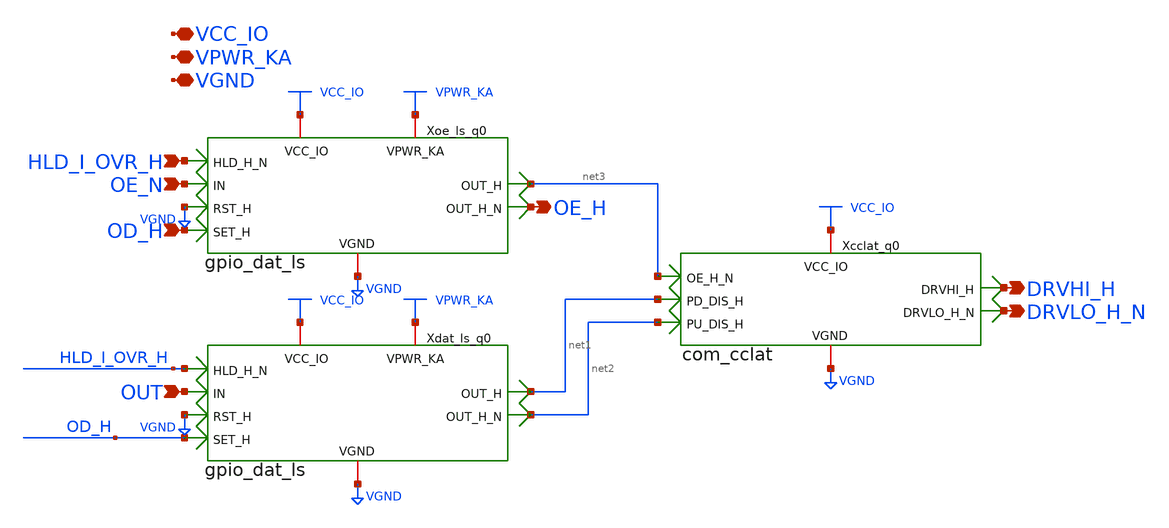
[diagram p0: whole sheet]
** sch_path: gpiov2_opath_datoe.sch
* Copyright 2023 David Mitchell Bailey
* Licensed under the Apache License, Version 2.0 (the "License");
* you may not use this file except in compliance with the License.
* You may obtain a copy of the License at
* https://www.apache.org/licenses/LICENSE-2.0
* Unless required by applicable law or agreed to in writing, software
* distributed under the License is distributed on an "AS IS" BASIS,
* WITHOUT WARRANTIES OR CONDITIONS OF ANY KIND, either express or implied.
* See the License for the specific language governing permissions and
* limitations under the License.
**.subckt gpiov2_opath_datoe VCC_IO DRVHI_H OUT HLD_I_OVR_H OE_N OD_H DRVLO_H_N OE_H VPWR_KA VGND
*.iopin VCC_IO
*.opin DRVHI_H
*.ipin OUT
*.ipin HLD_I_OVR_H
*.ipin OE_N
*.ipin OD_H
*.opin DRVLO_H_N
*.opin OE_H
*.iopin VPWR_KA
*.iopin VGND
Xdat_ls_q0 VCC_IO VPWR_KA VGND net1 net2 HLD_I_OVR_H OD_H VGND OUT gpio_dat_ls
Xcclat_q0 VCC_IO VGND DRVHI_H net2 net3 DRVLO_H_N net1 com_cclat
Xoe_ls_q0 VCC_IO VPWR_KA VGND net3 OE_H HLD_I_OVR_H OD_H VGND OE_N gpio_dat_ls
**.ends

* expanding   symbol:  gpio_dat_ls.sym # of pins=9
** sym_path: gpio_dat_ls.sym
** sch_path: gpio_dat_ls.sch
.subckt gpio_dat_ls VCC_IO VPWR_KA VGND OUT_H OUT_H_N HLD_H_N SET_H RST_H IN
*.ipin IN
*.ipin HLD_H_N
*.ipin SET_H
*.ipin RST_H
*.opin OUT_H_N
*.opin OUT_H
*.iopin VCC_IO
*.iopin VPWR_KA
*.iopin VGND
XM1 fbk fbk_n VGND VGND sky130_fd_pr__nfet_g5v0d10v5 L=0.6 W=0.7 nf=1 ad='int((nf+1)/2) * W/nf * 0.29'
+ as='int((nf+2)/2) * W/nf * 0.29' pd='2*int((nf+1)/2) * (W/nf + 0.29)' ps='2*int((nf+2)/2) * (W/nf + 0.29)'
+ nrd='0.29 / W' nrs='0.29 / W' sa=0 sb=0 sd=0 mult=1 m=1
XM2 fbk_n fbk VGND VGND sky130_fd_pr__nfet_g5v0d10v5 L=0.6 W=0.7 nf=1 ad='int((nf+1)/2) * W/nf * 0.29'
+ as='int((nf+2)/2) * W/nf * 0.29' pd='2*int((nf+1)/2) * (W/nf + 0.29)' ps='2*int((nf+2)/2) * (W/nf + 0.29)'
+ nrd='0.29 / W' nrs='0.29 / W' sa=0 sb=0 sd=0 mult=1 m=1
XM3 fbk fbk_n VCC_IO VCC_IO sky130_fd_pr__pfet_g5v0d10v5 L=0.5 W=1 nf=1 ad='int((nf+1)/2) * W/nf * 0.29'
+ as='int((nf+2)/2) * W/nf * 0.29' pd='2*int((nf+1)/2) * (W/nf + 0.29)' ps='2*int((nf+2)/2) * (W/nf + 0.29)'
+ nrd='0.29 / W' nrs='0.29 / W' sa=0 sb=0 sd=0 mult=1 m=1
XM4 fbk_n fbk VCC_IO VCC_IO sky130_fd_pr__pfet_g5v0d10v5 L=0.5 W=1 nf=1 ad='int((nf+1)/2) * W/nf * 0.29'
+ as='int((nf+2)/2) * W/nf * 0.29' pd='2*int((nf+1)/2) * (W/nf + 0.29)' ps='2*int((nf+2)/2) * (W/nf + 0.29)'
+ nrd='0.29 / W' nrs='0.29 / W' sa=0 sb=0 sd=0 mult=1 m=1
XM5 fbk HLD_H_N net3 VGND sky130_fd_pr__nfet_g5v0d10v5 L=0.5 W=5 nf=1 ad='int((nf+1)/2) * W/nf * 0.29'
+ as='int((nf+2)/2) * W/nf * 0.29' pd='2*int((nf+1)/2) * (W/nf + 0.29)' ps='2*int((nf+2)/2) * (W/nf + 0.29)'
+ nrd='0.29 / W' nrs='0.29 / W' sa=0 sb=0 sd=0 mult=1 m=1
XM6 net3 VPWR_KA net4 VGND sky130_fd_pr__nfet_05v0_nvt L=0.9 W=1 nf=1 ad='int((nf+1)/2) * W/nf * 0.29'
+ as='int((nf+2)/2) * W/nf * 0.29' pd='2*int((nf+1)/2) * (W/nf + 0.29)' ps='2*int((nf+2)/2) * (W/nf + 0.29)'
+ nrd='0.29 / W' nrs='0.29 / W' sa=0 sb=0 sd=0 mult=8 m=8
XM7 net4 net2 VGND VGND sky130_fd_pr__nfet_01v8_lvt L=0.15 W=8 nf=1 ad='int((nf+1)/2) * W/nf * 0.29'
+ as='int((nf+2)/2) * W/nf * 0.29' pd='2*int((nf+1)/2) * (W/nf + 0.29)' ps='2*int((nf+2)/2) * (W/nf + 0.29)'
+ nrd='0.29 / W' nrs='0.29 / W' sa=0 sb=0 sd=0 mult=1 m=1
XM8 fbk_n HLD_H_N net5 VGND sky130_fd_pr__nfet_g5v0d10v5 L=0.5 W=5 nf=1 ad='int((nf+1)/2) * W/nf * 0.29'
+ as='int((nf+2)/2) * W/nf * 0.29' pd='2*int((nf+1)/2) * (W/nf + 0.29)' ps='2*int((nf+2)/2) * (W/nf + 0.29)'
+ nrd='0.29 / W' nrs='0.29 / W' sa=0 sb=0 sd=0 mult=1 m=1
XM9 net5 VPWR_KA net6 VGND sky130_fd_pr__nfet_05v0_nvt L=0.9 W=1 nf=1 ad='int((nf+1)/2) * W/nf * 0.29'
+ as='int((nf+2)/2) * W/nf * 0.29' pd='2*int((nf+1)/2) * (W/nf + 0.29)' ps='2*int((nf+2)/2) * (W/nf + 0.29)'
+ nrd='0.29 / W' nrs='0.29 / W' sa=0 sb=0 sd=0 mult=8 m=8
XM10 net6 net1 VGND VGND sky130_fd_pr__nfet_01v8_lvt L=0.15 W=8 nf=1 ad='int((nf+1)/2) * W/nf * 0.29'
+ as='int((nf+2)/2) * W/nf * 0.29' pd='2*int((nf+1)/2) * (W/nf + 0.29)' ps='2*int((nf+2)/2) * (W/nf + 0.29)'
+ nrd='0.29 / W' nrs='0.29 / W' sa=0 sb=0 sd=0 mult=1 m=1
XM11 fbk SET_H VGND VGND sky130_fd_pr__nfet_g5v0d10v5 L=0.6 W=3 nf=1 ad='int((nf+1)/2) * W/nf * 0.29'
+ as='int((nf+2)/2) * W/nf * 0.29' pd='2*int((nf+1)/2) * (W/nf + 0.29)' ps='2*int((nf+2)/2) * (W/nf + 0.29)'
+ nrd='0.29 / W' nrs='0.29 / W' sa=0 sb=0 sd=0 mult=1 m=1
XM12 net1 IN VGND VGND sky130_fd_pr__nfet_01v8 L=0.25 W=1 nf=1 ad='int((nf+1)/2) * W/nf * 0.29' as='int((nf+2)/2) * W/nf * 0.29'
+ pd='2*int((nf+1)/2) * (W/nf + 0.29)' ps='2*int((nf+2)/2) * (W/nf + 0.29)' nrd='0.29 / W' nrs='0.29 / W'
+ sa=0 sb=0 sd=0 mult=2 m=2
XM14 net2 net1 VGND VGND sky130_fd_pr__nfet_01v8 L=0.25 W=1 nf=1 ad='int((nf+1)/2) * W/nf * 0.29' as='int((nf+2)/2) * W/nf * 0.29'
+ pd='2*int((nf+1)/2) * (W/nf + 0.29)' ps='2*int((nf+2)/2) * (W/nf + 0.29)' nrd='0.29 / W' nrs='0.29 / W'
+ sa=0 sb=0 sd=0 mult=2 m=2
XM16 fbk_n RST_H VGND VGND sky130_fd_pr__nfet_g5v0d10v5 L=0.6 W=3 nf=1 ad='int((nf+1)/2) * W/nf * 0.29'
+ as='int((nf+2)/2) * W/nf * 0.29' pd='2*int((nf+1)/2) * (W/nf + 0.29)' ps='2*int((nf+2)/2) * (W/nf + 0.29)'
+ nrd='0.29 / W' nrs='0.29 / W' sa=0 sb=0 sd=0 mult=1 m=1
XM17 OUT_H fbk VGND VGND sky130_fd_pr__nfet_g5v0d10v5 L=0.6 W=1 nf=1 ad='int((nf+1)/2) * W/nf * 0.29'
+ as='int((nf+2)/2) * W/nf * 0.29' pd='2*int((nf+1)/2) * (W/nf + 0.29)' ps='2*int((nf+2)/2) * (W/nf + 0.29)'
+ nrd='0.29 / W' nrs='0.29 / W' sa=0 sb=0 sd=0 mult=1 m=1
XM18 OUT_H fbk VCC_IO VCC_IO sky130_fd_pr__pfet_g5v0d10v5 L=0.5 W=3 nf=1 ad='int((nf+1)/2) * W/nf * 0.29'
+ as='int((nf+2)/2) * W/nf * 0.29' pd='2*int((nf+1)/2) * (W/nf + 0.29)' ps='2*int((nf+2)/2) * (W/nf + 0.29)'
+ nrd='0.29 / W' nrs='0.29 / W' sa=0 sb=0 sd=0 mult=1 m=1
XM19 OUT_H_N fbk_n VGND VGND sky130_fd_pr__nfet_g5v0d10v5 L=0.6 W=1 nf=1 ad='int((nf+1)/2) * W/nf * 0.29'
+ as='int((nf+2)/2) * W/nf * 0.29' pd='2*int((nf+1)/2) * (W/nf + 0.29)' ps='2*int((nf+2)/2) * (W/nf + 0.29)'
+ nrd='0.29 / W' nrs='0.29 / W' sa=0 sb=0 sd=0 mult=1 m=1
XM20 OUT_H_N fbk_n VCC_IO VCC_IO sky130_fd_pr__pfet_g5v0d10v5 L=0.5 W=3 nf=1 ad='int((nf+1)/2) * W/nf * 0.29'
+ as='int((nf+2)/2) * W/nf * 0.29' pd='2*int((nf+1)/2) * (W/nf + 0.29)' ps='2*int((nf+2)/2) * (W/nf + 0.29)'
+ nrd='0.29 / W' nrs='0.29 / W' sa=0 sb=0 sd=0 mult=1 m=1
XM13 net1 IN VPWR_KA VPWR_KA sky130_fd_pr__pfet_01v8_hvt L=0.25 W=3 nf=1 ad='int((nf+1)/2) * W/nf * 0.29'
+ as='int((nf+2)/2) * W/nf * 0.29' pd='2*int((nf+1)/2) * (W/nf + 0.29)' ps='2*int((nf+2)/2) * (W/nf + 0.29)'
+ nrd='0.29 / W' nrs='0.29 / W' sa=0 sb=0 sd=0 mult=1 m=1
XM15 net2 net1 VPWR_KA VPWR_KA sky130_fd_pr__pfet_01v8_hvt L=0.25 W=3 nf=1 ad='int((nf+1)/2) * W/nf * 0.29'
+ as='int((nf+2)/2) * W/nf * 0.29' pd='2*int((nf+1)/2) * (W/nf + 0.29)' ps='2*int((nf+2)/2) * (W/nf + 0.29)'
+ nrd='0.29 / W' nrs='0.29 / W' sa=0 sb=0 sd=0 mult=1 m=1
.ends


* expanding   symbol:  com_cclat.sym # of pins=7
** sym_path: com_cclat.sym
** sch_path: com_cclat.sch
.subckt com_cclat VCC_IO VGND DRVHI_H PU_DIS_H OE_H_N DRVLO_H_N PD_DIS_H
*.ipin PU_DIS_H
*.iopin VCC_IO
*.opin DRVHI_H
*.ipin OE_H_N
*.ipin PD_DIS_H
*.opin DRVLO_H_N
*.iopin VGND
x1 OE_H_N net1 VCC_IO VGND com_cclat_inv_in
x2 net1 net3 VCC_IO VGND com_cclat_inv_in
x3 PU_DIS_H net2 VCC_IO VGND com_cclat_inv_in
XI1 net1 DRVLO_H_N net2 net4 VCC_IO VGND com_cclat_hvnand3
XI2 net3 DRVHI_H PD_DIS_H net5 VCC_IO VGND com_cclat_hvnor3
x4 net4 DRVHI_H VCC_IO VGND com_cclat_inv_out
x5 net5 DRVLO_H_N VCC_IO VGND com_cclat_inv_out
.ends


* expanding   symbol:  com_cclat_inv_in.sym # of pins=4
** sym_path: com_cclat_inv_in.sym
** sch_path: com_cclat_inv_in.sch
.subckt com_cclat_inv_in IN OUT VCC_IO VGND
*.ipin IN
*.opin OUT
*.iopin VCC_IO
*.iopin VGND
XI1 OUT IN VGND VGND sky130_fd_pr__nfet_g5v0d10v5 L=0.6 W=3 nf=1 ad='int((nf+1)/2) * W/nf * 0.29' as='int((nf+2)/2) * W/nf * 0.29'
+ pd='2*int((nf+1)/2) * (W/nf + 0.29)' ps='2*int((nf+2)/2) * (W/nf + 0.29)' nrd='0.29 / W' nrs='0.29 / W'
+ sa=0 sb=0 sd=0 mult=1 m=1
XI2 OUT IN VCC_IO VCC_IO sky130_fd_pr__pfet_g5v0d10v5 L=0.5 W=5 nf=1 ad='int((nf+1)/2) * W/nf * 0.29'
+ as='int((nf+2)/2) * W/nf * 0.29' pd='2*int((nf+1)/2) * (W/nf + 0.29)' ps='2*int((nf+2)/2) * (W/nf + 0.29)'
+ nrd='0.29 / W' nrs='0.29 / W' sa=0 sb=0 sd=0 mult=1 m=1
.ends


* expanding   symbol:  com_cclat_hvnand3.sym # of pins=6
** sym_path: com_cclat_hvnand3.sym
** sch_path: com_cclat_hvnand3.sch
.subckt com_cclat_hvnand3 IN0 IN1 IN2 OUT VCC_IO VGND
*.ipin IN2
*.opin OUT
*.iopin VCC_IO
*.iopin VGND
*.ipin IN1
*.ipin IN0
XI1 OUT IN2 net1 VGND sky130_fd_pr__nfet_g5v0d10v5 L=0.6 W=3 nf=1 ad='int((nf+1)/2) * W/nf * 0.29' as='int((nf+2)/2) * W/nf * 0.29'
+ pd='2*int((nf+1)/2) * (W/nf + 0.29)' ps='2*int((nf+2)/2) * (W/nf + 0.29)' nrd='0.29 / W' nrs='0.29 / W'
+ sa=0 sb=0 sd=0 mult=2 m=2
XI5 OUT IN2 VCC_IO VCC_IO sky130_fd_pr__pfet_g5v0d10v5 L=0.5 W=5 nf=1 ad='int((nf+1)/2) * W/nf * 0.29'
+ as='int((nf+2)/2) * W/nf * 0.29' pd='2*int((nf+1)/2) * (W/nf + 0.29)' ps='2*int((nf+2)/2) * (W/nf + 0.29)'
+ nrd='0.29 / W' nrs='0.29 / W' sa=0 sb=0 sd=0 mult=1 m=1
XI3 OUT IN1 VCC_IO VCC_IO sky130_fd_pr__pfet_g5v0d10v5 L=0.5 W=5 nf=1 ad='int((nf+1)/2) * W/nf * 0.29'
+ as='int((nf+2)/2) * W/nf * 0.29' pd='2*int((nf+1)/2) * (W/nf + 0.29)' ps='2*int((nf+2)/2) * (W/nf + 0.29)'
+ nrd='0.29 / W' nrs='0.29 / W' sa=0 sb=0 sd=0 mult=1 m=1
XI6 net1 IN1 net2 VGND sky130_fd_pr__nfet_g5v0d10v5 L=0.6 W=3 nf=1 ad='int((nf+1)/2) * W/nf * 0.29' as='int((nf+2)/2) * W/nf * 0.29'
+ pd='2*int((nf+1)/2) * (W/nf + 0.29)' ps='2*int((nf+2)/2) * (W/nf + 0.29)' nrd='0.29 / W' nrs='0.29 / W'
+ sa=0 sb=0 sd=0 mult=2 m=2
XI2 net2 IN0 VGND VGND sky130_fd_pr__nfet_g5v0d10v5 L=0.6 W=3 nf=1 ad='int((nf+1)/2) * W/nf * 0.29' as='int((nf+2)/2) * W/nf * 0.29'
+ pd='2*int((nf+1)/2) * (W/nf + 0.29)' ps='2*int((nf+2)/2) * (W/nf + 0.29)' nrd='0.29 / W' nrs='0.29 / W'
+ sa=0 sb=0 sd=0 mult=4 m=4
XI4 OUT IN0 VCC_IO VCC_IO sky130_fd_pr__pfet_g5v0d10v5 L=0.5 W=5 nf=1 ad='int((nf+1)/2) * W/nf * 0.29'
+ as='int((nf+2)/2) * W/nf * 0.29' pd='2*int((nf+1)/2) * (W/nf + 0.29)' ps='2*int((nf+2)/2) * (W/nf + 0.29)'
+ nrd='0.29 / W' nrs='0.29 / W' sa=0 sb=0 sd=0 mult=1 m=1
.ends


* expanding   symbol:  com_cclat_hvnor3.sym # of pins=6
** sym_path: com_cclat_hvnor3.sym
** sch_path: com_cclat_hvnor3.sch
.subckt com_cclat_hvnor3 IN0 IN1 IN2 OUT VCC_IO VGND
*.ipin IN2
*.opin OUT
*.iopin VCC_IO
*.iopin VGND
*.ipin IN0
*.ipin IN1
XI2 OUT IN2 VGND VGND sky130_fd_pr__nfet_g5v0d10v5 L=0.6 W=3 nf=1 ad='int((nf+1)/2) * W/nf * 0.29' as='int((nf+2)/2) * W/nf * 0.29'
+ pd='2*int((nf+1)/2) * (W/nf + 0.29)' ps='2*int((nf+2)/2) * (W/nf + 0.29)' nrd='0.29 / W' nrs='0.29 / W'
+ sa=0 sb=0 sd=0 mult=2 m=2
XI1 OUT IN2 net1 VCC_IO sky130_fd_pr__pfet_g5v0d10v5 L=0.5 W=5 nf=1 ad='int((nf+1)/2) * W/nf * 0.29'
+ as='int((nf+2)/2) * W/nf * 0.29' pd='2*int((nf+1)/2) * (W/nf + 0.29)' ps='2*int((nf+2)/2) * (W/nf + 0.29)'
+ nrd='0.29 / W' nrs='0.29 / W' sa=0 sb=0 sd=0 mult=4 m=4
XI3 net2 IN0 VCC_IO VCC_IO sky130_fd_pr__pfet_g5v0d10v5 L=0.6 W=5 nf=1 ad='int((nf+1)/2) * W/nf * 0.29'
+ as='int((nf+2)/2) * W/nf * 0.29' pd='2*int((nf+1)/2) * (W/nf + 0.29)' ps='2*int((nf+2)/2) * (W/nf + 0.29)'
+ nrd='0.29 / W' nrs='0.29 / W' sa=0 sb=0 sd=0 mult=8 m=8
XI4 OUT IN0 VGND VGND sky130_fd_pr__nfet_g5v0d10v5 L=0.6 W=3 nf=1 ad='int((nf+1)/2) * W/nf * 0.29' as='int((nf+2)/2) * W/nf * 0.29'
+ pd='2*int((nf+1)/2) * (W/nf + 0.29)' ps='2*int((nf+2)/2) * (W/nf + 0.29)' nrd='0.29 / W' nrs='0.29 / W'
+ sa=0 sb=0 sd=0 mult=2 m=2
XI5 net1 IN1 net2 VCC_IO sky130_fd_pr__pfet_g5v0d10v5 L=0.5 W=5 nf=1 ad='int((nf+1)/2) * W/nf * 0.29'
+ as='int((nf+2)/2) * W/nf * 0.29' pd='2*int((nf+1)/2) * (W/nf + 0.29)' ps='2*int((nf+2)/2) * (W/nf + 0.29)'
+ nrd='0.29 / W' nrs='0.29 / W' sa=0 sb=0 sd=0 mult=4 m=4
XI6 OUT IN1 VGND VGND sky130_fd_pr__nfet_g5v0d10v5 L=0.6 W=3 nf=1 ad='int((nf+1)/2) * W/nf * 0.29' as='int((nf+2)/2) * W/nf * 0.29'
+ pd='2*int((nf+1)/2) * (W/nf + 0.29)' ps='2*int((nf+2)/2) * (W/nf + 0.29)' nrd='0.29 / W' nrs='0.29 / W'
+ sa=0 sb=0 sd=0 mult=2 m=2
.ends


* expanding   symbol:  com_cclat_inv_out.sym # of pins=4
** sym_path: com_cclat_inv_out.sym
** sch_path: com_cclat_inv_out.sch
.subckt com_cclat_inv_out IN OUT VCC_IO VGND
*.ipin IN
*.opin OUT
*.iopin VCC_IO
*.iopin VGND
XI1 OUT IN VGND VGND sky130_fd_pr__nfet_g5v0d10v5 L=0.6 W=3 nf=1 ad='int((nf+1)/2) * W/nf * 0.29' as='int((nf+2)/2) * W/nf * 0.29'
+ pd='2*int((nf+1)/2) * (W/nf + 0.29)' ps='2*int((nf+2)/2) * (W/nf + 0.29)' nrd='0.29 / W' nrs='0.29 / W'
+ sa=0 sb=0 sd=0 mult=6 m=6
XI2 OUT IN VCC_IO VCC_IO sky130_fd_pr__pfet_g5v0d10v5 L=0.5 W=5 nf=1 ad='int((nf+1)/2) * W/nf * 0.29'
+ as='int((nf+2)/2) * W/nf * 0.29' pd='2*int((nf+1)/2) * (W/nf + 0.29)' ps='2*int((nf+2)/2) * (W/nf + 0.29)'
+ nrd='0.29 / W' nrs='0.29 / W' sa=0 sb=0 sd=0 mult=6 m=6
.ends

.end
